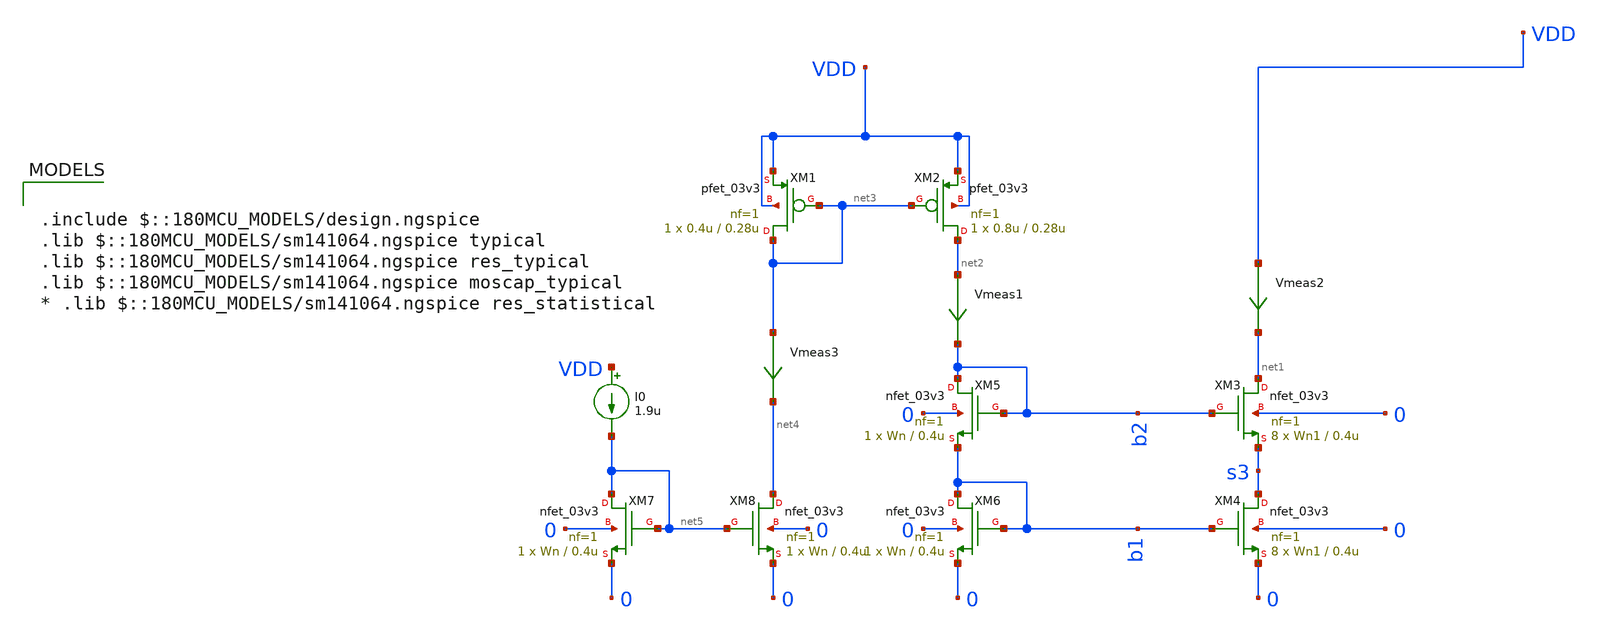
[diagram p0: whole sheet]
** sch_path: DAC/xschem/analog_cell/test/test)cascode_current_mirror.sch
**.subckt test)cascode_current_mirror
XM3 net1 b2 s3 0 nfet_03v3 L=0.4u W=Wn1 nf=1 ad='int((nf+1)/2) * W/nf * 0.18u' as='int((nf+2)/2) * W/nf * 0.18u'
+ pd='2*int((nf+1)/2) * (W/nf + 0.18u)' ps='2*int((nf+2)/2) * (W/nf + 0.18u)' nrd='0.18u / W' nrs='0.18u / W'
+ sa=0 sb=0 sd=0 m=8
XM4 s3 b1 0 0 nfet_03v3 L=0.4u W=Wn1 nf=1 ad='int((nf+1)/2) * W/nf * 0.18u' as='int((nf+2)/2) * W/nf * 0.18u'
+ pd='2*int((nf+1)/2) * (W/nf + 0.18u)' ps='2*int((nf+2)/2) * (W/nf + 0.18u)' nrd='0.18u / W' nrs='0.18u / W'
+ sa=0 sb=0 sd=0 m=8
XM5 b2 b2 b1 0 nfet_03v3 L=0.4u W=Wn nf=1 ad='int((nf+1)/2) * W/nf * 0.18u' as='int((nf+2)/2) * W/nf * 0.18u'
+ pd='2*int((nf+1)/2) * (W/nf + 0.18u)' ps='2*int((nf+2)/2) * (W/nf + 0.18u)' nrd='0.18u / W' nrs='0.18u / W'
+ sa=0 sb=0 sd=0 m=1
XM6 b1 b1 0 0 nfet_03v3 L=0.4u W=Wn nf=1 ad='int((nf+1)/2) * W/nf * 0.18u' as='int((nf+2)/2) * W/nf * 0.18u'
+ pd='2*int((nf+1)/2) * (W/nf + 0.18u)' ps='2*int((nf+2)/2) * (W/nf + 0.18u)' nrd='0.18u / W' nrs='0.18u / W'
+ sa=0 sb=0 sd=0 m=1
I0 VDD net5 1.9u
Vmeas2 VDD net1 0
.save i(vmeas2)
Vmeas1 net2 b2 0
.save i(vmeas1)
XM1 net3 net3 VDD VDD pfet_03v3 L=0.28u W=0.4u nf=1 ad='int((nf+1)/2) * W/nf * 0.18u' as='int((nf+2)/2) * W/nf * 0.18u'
+ pd='2*int((nf+1)/2) * (W/nf + 0.18u)' ps='2*int((nf+2)/2) * (W/nf + 0.18u)' nrd='0.18u / W' nrs='0.18u / W'
+ sa=0 sb=0 sd=0 m=1
XM2 net2 net3 VDD VDD pfet_03v3 L=0.28u W=0.8u nf=1 ad='int((nf+1)/2) * W/nf * 0.18u' as='int((nf+2)/2) * W/nf * 0.18u'
+ pd='2*int((nf+1)/2) * (W/nf + 0.18u)' ps='2*int((nf+2)/2) * (W/nf + 0.18u)' nrd='0.18u / W' nrs='0.18u / W'
+ sa=0 sb=0 sd=0 m=1
Vmeas3 net3 net4 0
.save i(vmeas3)
XM7 net5 net5 0 0 nfet_03v3 L=0.4u W=Wn nf=1 ad='int((nf+1)/2) * W/nf * 0.18u' as='int((nf+2)/2) * W/nf * 0.18u'
+ pd='2*int((nf+1)/2) * (W/nf + 0.18u)' ps='2*int((nf+2)/2) * (W/nf + 0.18u)' nrd='0.18u / W' nrs='0.18u / W'
+ sa=0 sb=0 sd=0 m=1
XM8 net4 net5 0 0 nfet_03v3 L=0.4u W=Wn nf=1 ad='int((nf+1)/2) * W/nf * 0.18u' as='int((nf+2)/2) * W/nf * 0.18u'
+ pd='2*int((nf+1)/2) * (W/nf + 0.18u)' ps='2*int((nf+2)/2) * (W/nf + 0.18u)' nrd='0.18u / W' nrs='0.18u / W'
+ sa=0 sb=0 sd=0 m=1
**** begin user architecture code

.include $::180MCU_MODELS/design.ngspice
.lib $::180MCU_MODELS/sm141064.ngspice typical
.lib $::180MCU_MODELS/sm141064.ngspice res_typical
.lib $::180MCU_MODELS/sm141064.ngspice moscap_typical
* .lib $::180MCU_MODELS/sm141064.ngspice res_statistical



V0 VDD 0 3
V1 IN+ 0 3
V2 IN- 0 0

.options savecurrents
.param Wn=0.3u
.param Wn1=0.3u
.save @m.xm1.m0[vth] @m.xm2.m0[vth] @m.xm3.m0[vth] @m.xm4.m0[vth]
.control
	dc I0 0u 2u 0.1u
	plot v(b1) v(s3)
	plot v(b2) v(VDD)
	*plot v(VDD)-v(s3)-(v(b2)-v(s3)-@m.xm3.m0[vth])
	plot i(Vmeas1) i(Vmeas2) i(Vmeas3)
	*tran 1u 100u
 	plot v(b2)-v(s3)-@m.xm3.m0[vth] v(b1)-@m.xm4.m0[vth]
	*plot v(s3) v(VDD)-V(s3)
	plot @m.xm3.m0[vth] @m.xm4.m0[vth]
.endc

.save all @m.xm1.m0[vth] @m.xm2.m0[vth] @m.xm3.m0[vth] @m.xm4.m0[vth]


**** end user architecture code
**.ends
.end
